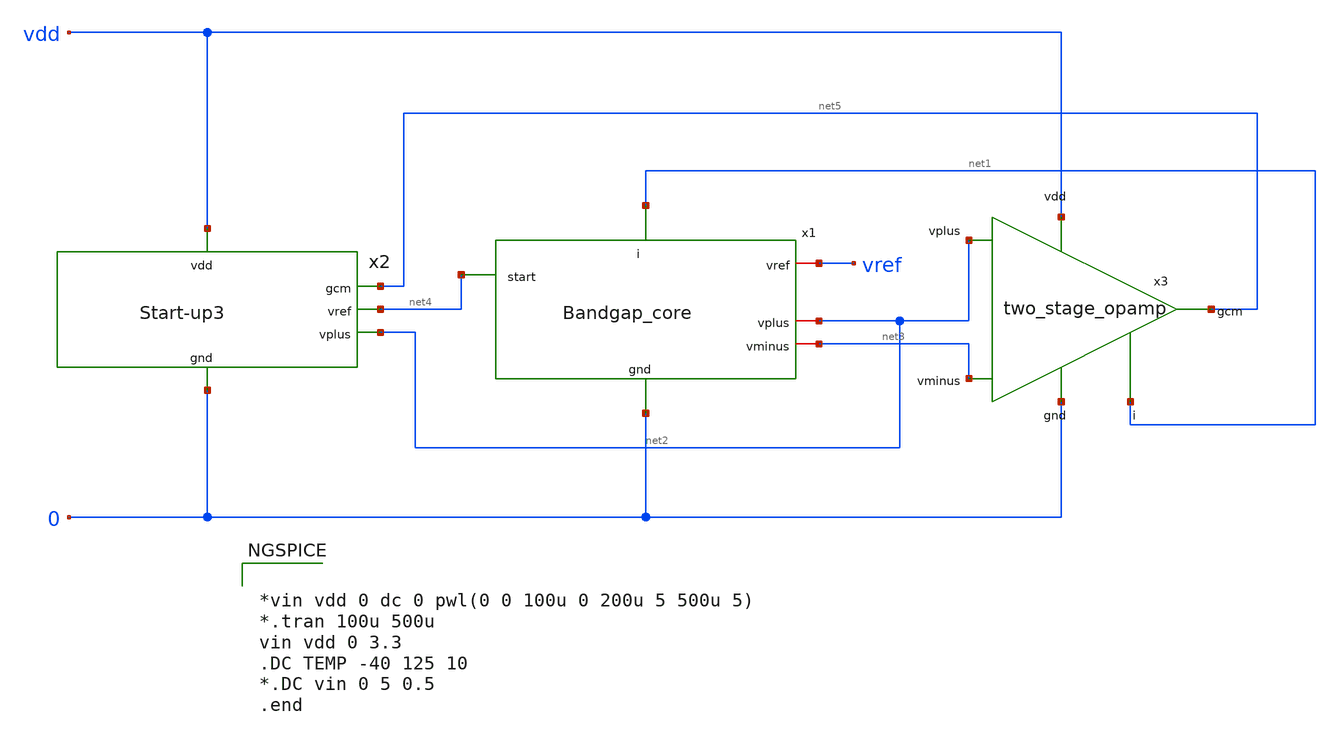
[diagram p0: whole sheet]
** sch_path: Bandgap/My Design/Schematics/Bandgap.sch
**.subckt Bandgap
x1 net1 net4 vref net2 net3 0 Bandgap_core
x2 vdd net5 net4 net2 0 Start-up3
x3 vdd net5 net2 net1 net3 0 two_stage_opamp
**** begin user architecture code

.include $::SKYWATER_MODELS/cells/nfet_01v8/sky130_fd_pr__nfet_01v8__tt.corner.spice
.include $::SKYWATER_MODELS/cells/nfet_01v8_lvt/sky130_fd_pr__nfet_01v8_lvt__tt.corner.spice
.include $::SKYWATER_MODELS/cells/pfet_01v8/sky130_fd_pr__pfet_01v8__tt.corner.spice
.include $::SKYWATER_MODELS/cells/nfet_03v3_nvt/sky130_fd_pr__nfet_03v3_nvt__tt.corner.spice
.include $::SKYWATER_MODELS/cells/nfet_05v0_nvt/sky130_fd_pr__nfet_05v0_nvt__tt.corner.spice
.include $::SKYWATER_MODELS/cells/esd_nfet_01v8/sky130_fd_pr__esd_nfet_01v8__tt.corner.spice
.include $::SKYWATER_MODELS/cells/pfet_01v8_lvt/sky130_fd_pr__pfet_01v8_lvt__tt.corner.spice
.include $::SKYWATER_MODELS/cells/pfet_01v8_hvt/sky130_fd_pr__pfet_01v8_hvt__tt.corner.spice
.include $::SKYWATER_MODELS/cells/esd_pfet_g5v0d10v5/sky130_fd_pr__esd_pfet_g5v0d10v5__tt.corner.spice
.include $::SKYWATER_MODELS/cells/pfet_g5v0d10v5/sky130_fd_pr__pfet_g5v0d10v5__tt.corner.spice
.include $::SKYWATER_MODELS/cells/pfet_g5v0d16v0/sky130_fd_pr__pfet_g5v0d16v0__tt.corner.spice
.include $::SKYWATER_MODELS/cells/nfet_g5v0d10v5/sky130_fd_pr__nfet_g5v0d10v5__tt.corner.spice
.include $::SKYWATER_MODELS/cells/nfet_g5v0d16v0/sky130_fd_pr__nfet_g5v0d16v0__tt_discrete.corner.spice
.include $::SKYWATER_MODELS/cells/esd_nfet_g5v0d10v5/sky130_fd_pr__esd_nfet_g5v0d10v5__tt.corner.spice
.include $::SKYWATER_MODELS/models/corners/tt/nonfet.spice
* Mismatch parameters
.include $::SKYWATER_MODELS/cells/nfet_01v8/sky130_fd_pr__nfet_01v8__mismatch.corner.spice
.include $::SKYWATER_MODELS/cells/pfet_01v8/sky130_fd_pr__pfet_01v8__mismatch.corner.spice
.include $::SKYWATER_MODELS/cells/nfet_01v8_lvt/sky130_fd_pr__nfet_01v8_lvt__mismatch.corner.spice
.include $::SKYWATER_MODELS/cells/pfet_01v8_lvt/sky130_fd_pr__pfet_01v8_lvt__mismatch.corner.spice
.include $::SKYWATER_MODELS/cells/pfet_01v8_hvt/sky130_fd_pr__pfet_01v8_hvt__mismatch.corner.spice
.include $::SKYWATER_MODELS/cells/nfet_g5v0d10v5/sky130_fd_pr__nfet_g5v0d10v5__mismatch.corner.spice
.include $::SKYWATER_MODELS/cells/pfet_g5v0d10v5/sky130_fd_pr__pfet_g5v0d10v5__mismatch.corner.spice
.include $::SKYWATER_MODELS/cells/nfet_05v0_nvt/sky130_fd_pr__nfet_05v0_nvt__mismatch.corner.spice
.include $::SKYWATER_MODELS/cells/nfet_03v3_nvt/sky130_fd_pr__nfet_03v3_nvt__mismatch.corner.spice
* Resistor$::SKYWATER_MODELS/Capacitor
.include $::SKYWATER_MODELS/models/r+c/res_typical__cap_typical.spice
.include $::SKYWATER_MODELS/models/r+c/res_typical__cap_typical__lin.spice
* Special cells
.include $::SKYWATER_MODELS/models/corners/tt/specialized_cells.spice
* All models
.include $::SKYWATER_MODELS/models/all.spice
* Corner
.include $::SKYWATER_MODELS/models/corners/tt/rf.spice



*vin vdd 0 dc 0 pwl(0 0 100u 0 200u 5 500u 5)
*.tran 100u 500u
vin vdd 0 3.3
.DC TEMP -40 125 10
*.DC vin 0 5 0.5
.end


**** end user architecture code
**.ends
.end
